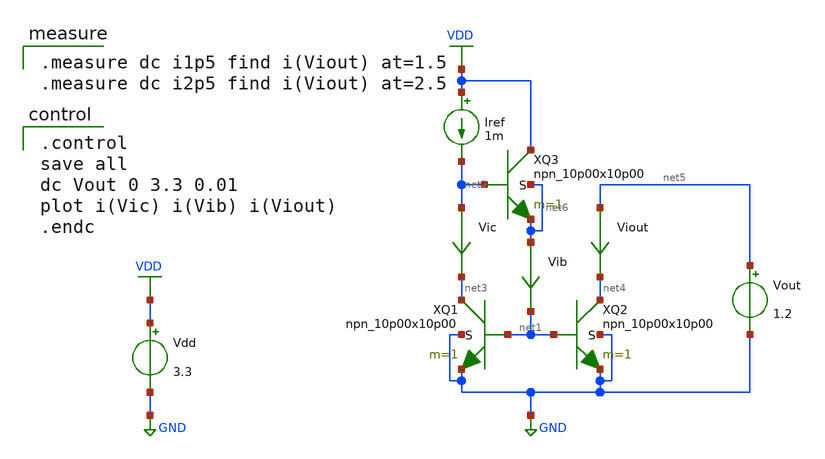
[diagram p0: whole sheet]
** sch_path: current-source/cm-ibcomp-bjt.sch
**.subckt cm-ibcomp-bjt
XQ2 net4 net1 GND GND npn_10p00x10p00 m=1
XQ1 net3 net1 GND GND npn_10p00x10p00 m=1
Viout net5 net4 0
.save i(viout)
Vdd VDD GND 3.3
Iref VDD net2 1m
Vic net2 net3 0
.save i(vic)
Vib net6 net1 0
.save i(vib)
Vout net5 GND 1.2
XQ3 VDD net2 net6 net6 npn_10p00x10p00 m=1
**** begin user architecture code

.include $::180MCU_MODELS/design.ngspice
.lib $::180MCU_MODELS/sm141064.ngspice typical
.lib $::180MCU_MODELS/sm141064.ngspice res_typical
.lib $::180MCU_MODELS/sm141064.ngspice moscap_typical
.lib $::180MCU_MODELS/sm141064.ngspice bjt_typical
* .lib $::180MCU_MODELS/sm141064.ngspice res_statistical


.control
save all
dc Vout 0 3.3 0.01
plot i(Vic) i(Vib) i(Viout)
.endc


.measure dc i1p5 find i(Viout) at=1.5
.measure dc i2p5 find i(Viout) at=2.5

**** end user architecture code
**.ends
.GLOBAL GND
.GLOBAL VDD
.end
